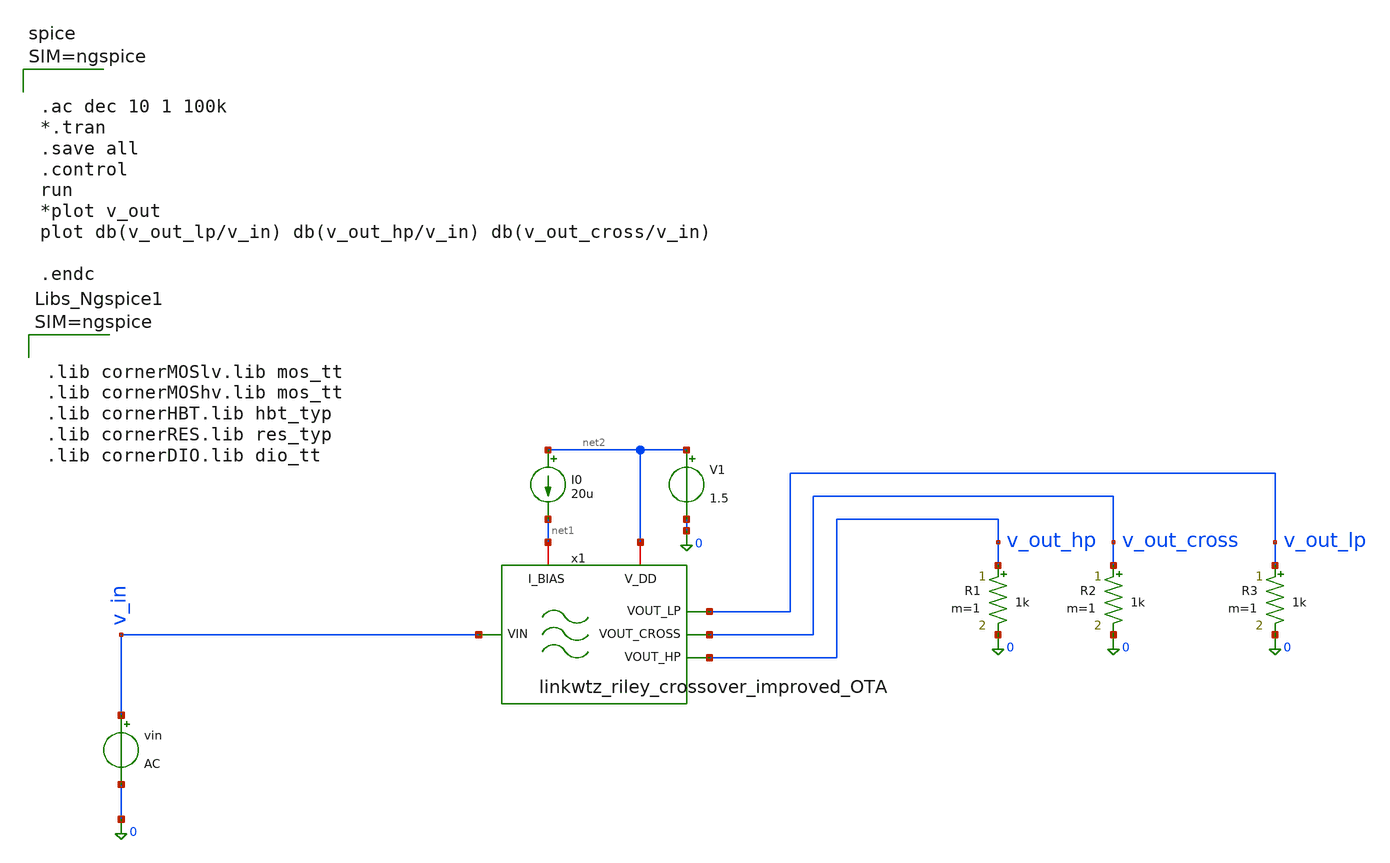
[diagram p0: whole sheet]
** sch_path: 004_Real_Circuits/linkwitz_riley_real_circ_top_tb.sch
**.subckt linkwitz_riley_real_circ_top_tb
vin v_in 0 AC
R2 v_out_cross 0 1k m=1
R3 v_out_lp 0 1k m=1
I0 net2 net1 20u
V1 net2 0 1.5
R1 v_out_hp 0 1k m=1
x1 net2 net1 v_out_lp v_in v_out_cross v_out_hp linkwtz_riley_crossover_improved_OTA
**** begin user architecture code



.lib cornerMOSlv.lib mos_tt
.lib cornerMOShv.lib mos_tt
.lib cornerHBT.lib hbt_typ
.lib cornerRES.lib res_typ
.lib cornerDIO.lib dio_tt






.ac dec 10 1 100k
*.tran
.save all
.control
run
*plot v_out
plot db(v_out_lp/v_in) db(v_out_hp/v_in) db(v_out_cross/v_in)

.endc



**** end user architecture code
**.ends

* expanding   symbol:  /foss/designs/004_Real_Circuits/linkwtz_riley_crossover_improved_OTA.sym # of
*+ pins=6
** sym_path: 004_Real_Circuits/linkwtz_riley_crossover_improved_OTA.sym
** sch_path: 004_Real_Circuits/linkwtz_riley_crossover_improved_OTA.sch
.subckt linkwtz_riley_crossover_improved_OTA V_DD I_BIAS VOUT_LP VIN VOUT_CROSS VOUT_HP
*.opin VOUT_LP
*.opin VOUT_HP
*.ipin VIN
*.iopin I_BIAS
*.iopin V_DD
*.opin VOUT_CROSS
x1 V_DD VOUT_LP I_BIAS net2 VOUT_LP 0 5T-OTA
x2 V_DD VOUT_HP I_BIAS net4 VOUT_HP 0 5T-OTA
R1 net1 VIN R_LP m=1
.param C_LP=1.06e-6
.param R_LP=1000
.param C_HP=1e-9
.param R_HP=1.06e6
.param R_IN=1k
R2 net2 net1 R_LP m=1
C1 net2 0 C_LP m=1
C2 net1 VOUT_LP C_LP m=1
C3 VIN net3 C_HP m=1
C4 net3 net4 C_HP m=1
R3 net3 VOUT_HP R_HP m=1
R4 net4 0 R_HP m=1
R10 net5 net6 R_IN m=1
R11 VOUT_HP net5 R_IN m=1
R12 net7 VOUT_CROSS R_IN m=1
R13 net6 net7 R_IN m=1
R14 VOUT_LP net7 R_IN m=1
E1 net6 0 0 net5 1e6
E4 VOUT_CROSS 0 0 net7 1e6
.ends


* expanding   symbol:  /foss/designs/Repo/004_Real_Circuits/5T-OTA.sym # of pins=6
** sym_path: 004_Real_Circuits/5T-OTA.sym
** sch_path: 004_Real_Circuits/5T-OTA.sch
.subckt 5T-OTA vdd vout ibias vinp vinn vss
*.ipin vinp
*.iopin vdd
*.iopin vss
*.opin vout
*.ipin vinn
*.iopin ibias
XM1 net3 vinp net1 net4 sg13_lv_nmos w=2u l=5u ng=1 m=1 mm_ok=1
XM5 net1 net2 vss vss sg13_lv_nmos w=0.5u l=5u ng=1 m=1 mm_ok=1
XM2 vout vinn net1 net5 sg13_lv_nmos w=2u l=5u ng=1 m=1 mm_ok=1
XM6 net2 net2 vss vss sg13_lv_nmos w=2.5u l=5u ng=1 m=1 mm_ok=1
XM3 net3 net3 vdd vdd sg13_lv_pmos w=1.5u l=5u ng=1 m=1 mm_ok=1
XM4 vout net3 vdd vdd sg13_lv_pmos w=1.5u l=5u ng=1 m=1 mm_ok=1
XM7 net2 ibias vdd net6 sg13_lv_pmos w=0.15u l=0.13u ng=1 m=1 mm_ok=1
.ends

.end
